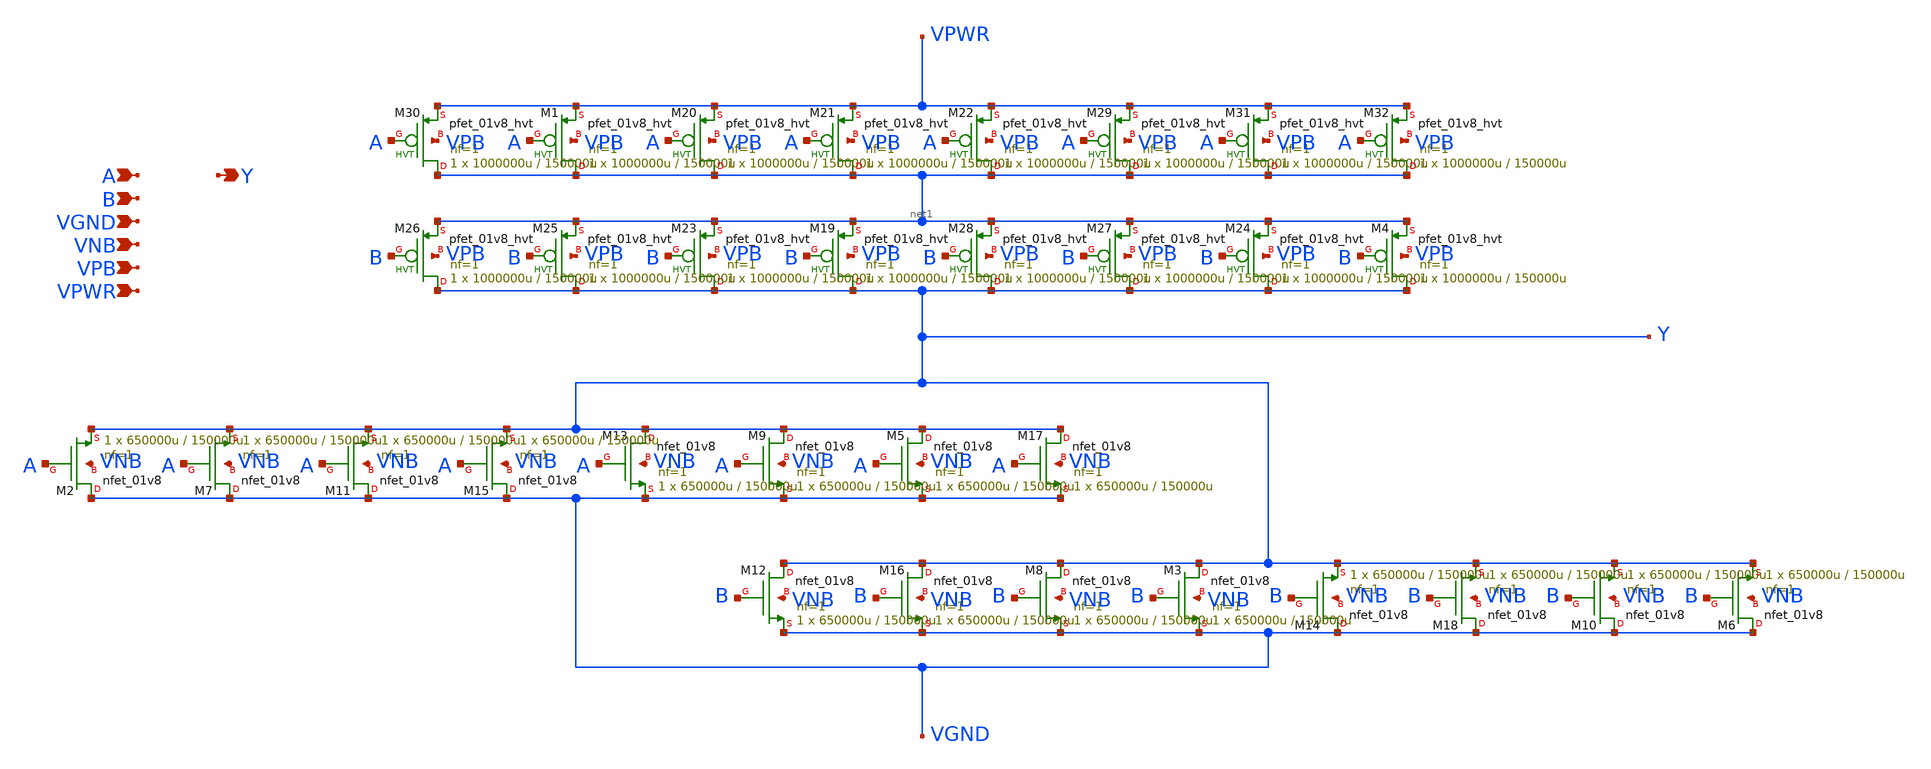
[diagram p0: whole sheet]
** sch_path: schematics/nor2/sky130_fd_sc_hd__nor2_8.sch
**.subckt sky130_fd_sc_hd__nor2_8 A B VGND VNB VPB VPWR Y
*.ipin A
*.ipin B
*.ipin VGND
*.ipin VNB
*.ipin VPB
*.ipin VPWR
*.opin Y
XM2 VGND A Y VNB sky130_fd_pr__nfet_01v8 L=150000u W=650000u nf=1 ad='int((1 + 1)/2) * 650000u / 1 * 0.29'
+ as='int((1 + 2)/2) * 650000u / 1 * 0.29' pd='2*int((1 + 1)/2) * (650000u / 1 + 0.29)' ps='2*int((1 + 2)/2) * (650000u / 1 + 0.29)'
+ nrd='0.29 / 650000u ' nrs='0.29 / 650000u ' sa=0 sb=0 sd=0 mult=1 m=1
XM3 Y B VGND VNB sky130_fd_pr__nfet_01v8 L=150000u W=650000u nf=1 ad='int((1 + 1)/2) * 650000u / 1 * 0.29'
+ as='int((1 + 2)/2) * 650000u / 1 * 0.29' pd='2*int((1 + 1)/2) * (650000u / 1 + 0.29)' ps='2*int((1 + 2)/2) * (650000u / 1 + 0.29)'
+ nrd='0.29 / 650000u ' nrs='0.29 / 650000u ' sa=0 sb=0 sd=0 mult=1 m=1
XM5 Y A VGND VNB sky130_fd_pr__nfet_01v8 L=150000u W=650000u nf=1 ad='int((1 + 1)/2) * 650000u / 1 * 0.29'
+ as='int((1 + 2)/2) * 650000u / 1 * 0.29' pd='2*int((1 + 1)/2) * (650000u / 1 + 0.29)' ps='2*int((1 + 2)/2) * (650000u / 1 + 0.29)'
+ nrd='0.29 / 650000u ' nrs='0.29 / 650000u ' sa=0 sb=0 sd=0 mult=1 m=1
XM6 VGND B Y VNB sky130_fd_pr__nfet_01v8 L=150000u W=650000u nf=1 ad='int((1 + 1)/2) * 650000u / 1 * 0.29'
+ as='int((1 + 2)/2) * 650000u / 1 * 0.29' pd='2*int((1 + 1)/2) * (650000u / 1 + 0.29)' ps='2*int((1 + 2)/2) * (650000u / 1 + 0.29)'
+ nrd='0.29 / 650000u ' nrs='0.29 / 650000u ' sa=0 sb=0 sd=0 mult=1 m=1
XM7 VGND A Y VNB sky130_fd_pr__nfet_01v8 L=150000u W=650000u nf=1 ad='int((1 + 1)/2) * 650000u / 1 * 0.29'
+ as='int((1 + 2)/2) * 650000u / 1 * 0.29' pd='2*int((1 + 1)/2) * (650000u / 1 + 0.29)' ps='2*int((1 + 2)/2) * (650000u / 1 + 0.29)'
+ nrd='0.29 / 650000u ' nrs='0.29 / 650000u ' sa=0 sb=0 sd=0 mult=1 m=1
XM8 Y B VGND VNB sky130_fd_pr__nfet_01v8 L=150000u W=650000u nf=1 ad='int((1 + 1)/2) * 650000u / 1 * 0.29'
+ as='int((1 + 2)/2) * 650000u / 1 * 0.29' pd='2*int((1 + 1)/2) * (650000u / 1 + 0.29)' ps='2*int((1 + 2)/2) * (650000u / 1 + 0.29)'
+ nrd='0.29 / 650000u ' nrs='0.29 / 650000u ' sa=0 sb=0 sd=0 mult=1 m=1
XM9 Y A VGND VNB sky130_fd_pr__nfet_01v8 L=150000u W=650000u nf=1 ad='int((1 + 1)/2) * 650000u / 1 * 0.29'
+ as='int((1 + 2)/2) * 650000u / 1 * 0.29' pd='2*int((1 + 1)/2) * (650000u / 1 + 0.29)' ps='2*int((1 + 2)/2) * (650000u / 1 + 0.29)'
+ nrd='0.29 / 650000u ' nrs='0.29 / 650000u ' sa=0 sb=0 sd=0 mult=1 m=1
XM10 VGND B Y VNB sky130_fd_pr__nfet_01v8 L=150000u W=650000u nf=1 ad='int((1 + 1)/2) * 650000u / 1 * 0.29'
+ as='int((1 + 2)/2) * 650000u / 1 * 0.29' pd='2*int((1 + 1)/2) * (650000u / 1 + 0.29)' ps='2*int((1 + 2)/2) * (650000u / 1 + 0.29)'
+ nrd='0.29 / 650000u ' nrs='0.29 / 650000u ' sa=0 sb=0 sd=0 mult=1 m=1
XM11 VGND A Y VNB sky130_fd_pr__nfet_01v8 L=150000u W=650000u nf=1 ad='int((1 + 1)/2) * 650000u / 1 * 0.29'
+ as='int((1 + 2)/2) * 650000u / 1 * 0.29' pd='2*int((1 + 1)/2) * (650000u / 1 + 0.29)' ps='2*int((1 + 2)/2) * (650000u / 1 + 0.29)'
+ nrd='0.29 / 650000u ' nrs='0.29 / 650000u ' sa=0 sb=0 sd=0 mult=1 m=1
XM12 Y B VGND VNB sky130_fd_pr__nfet_01v8 L=150000u W=650000u nf=1 ad='int((1 + 1)/2) * 650000u / 1 * 0.29'
+ as='int((1 + 2)/2) * 650000u / 1 * 0.29' pd='2*int((1 + 1)/2) * (650000u / 1 + 0.29)' ps='2*int((1 + 2)/2) * (650000u / 1 + 0.29)'
+ nrd='0.29 / 650000u ' nrs='0.29 / 650000u ' sa=0 sb=0 sd=0 mult=1 m=1
XM13 Y A VGND VNB sky130_fd_pr__nfet_01v8 L=150000u W=650000u nf=1 ad='int((1 + 1)/2) * 650000u / 1 * 0.29'
+ as='int((1 + 2)/2) * 650000u / 1 * 0.29' pd='2*int((1 + 1)/2) * (650000u / 1 + 0.29)' ps='2*int((1 + 2)/2) * (650000u / 1 + 0.29)'
+ nrd='0.29 / 650000u ' nrs='0.29 / 650000u ' sa=0 sb=0 sd=0 mult=1 m=1
XM14 VGND B Y VNB sky130_fd_pr__nfet_01v8 L=150000u W=650000u nf=1 ad='int((1 + 1)/2) * 650000u / 1 * 0.29'
+ as='int((1 + 2)/2) * 650000u / 1 * 0.29' pd='2*int((1 + 1)/2) * (650000u / 1 + 0.29)' ps='2*int((1 + 2)/2) * (650000u / 1 + 0.29)'
+ nrd='0.29 / 650000u ' nrs='0.29 / 650000u ' sa=0 sb=0 sd=0 mult=1 m=1
XM15 VGND A Y VNB sky130_fd_pr__nfet_01v8 L=150000u W=650000u nf=1 ad='int((1 + 1)/2) * 650000u / 1 * 0.29'
+ as='int((1 + 2)/2) * 650000u / 1 * 0.29' pd='2*int((1 + 1)/2) * (650000u / 1 + 0.29)' ps='2*int((1 + 2)/2) * (650000u / 1 + 0.29)'
+ nrd='0.29 / 650000u ' nrs='0.29 / 650000u ' sa=0 sb=0 sd=0 mult=1 m=1
XM16 Y B VGND VNB sky130_fd_pr__nfet_01v8 L=150000u W=650000u nf=1 ad='int((1 + 1)/2) * 650000u / 1 * 0.29'
+ as='int((1 + 2)/2) * 650000u / 1 * 0.29' pd='2*int((1 + 1)/2) * (650000u / 1 + 0.29)' ps='2*int((1 + 2)/2) * (650000u / 1 + 0.29)'
+ nrd='0.29 / 650000u ' nrs='0.29 / 650000u ' sa=0 sb=0 sd=0 mult=1 m=1
XM17 Y A VGND VNB sky130_fd_pr__nfet_01v8 L=150000u W=650000u nf=1 ad='int((1 + 1)/2) * 650000u / 1 * 0.29'
+ as='int((1 + 2)/2) * 650000u / 1 * 0.29' pd='2*int((1 + 1)/2) * (650000u / 1 + 0.29)' ps='2*int((1 + 2)/2) * (650000u / 1 + 0.29)'
+ nrd='0.29 / 650000u ' nrs='0.29 / 650000u ' sa=0 sb=0 sd=0 mult=1 m=1
XM18 VGND B Y VNB sky130_fd_pr__nfet_01v8 L=150000u W=650000u nf=1 ad='int((1 + 1)/2) * 650000u / 1 * 0.29'
+ as='int((1 + 2)/2) * 650000u / 1 * 0.29' pd='2*int((1 + 1)/2) * (650000u / 1 + 0.29)' ps='2*int((1 + 2)/2) * (650000u / 1 + 0.29)'
+ nrd='0.29 / 650000u ' nrs='0.29 / 650000u ' sa=0 sb=0 sd=0 mult=1 m=1
XM19 Y B net1 VPB sky130_fd_pr__pfet_01v8_hvt L=150000u W=1000000u nf=1 ad='int((1 + 1)/2) * 1000000u / 1 * 0.29'
+ as='int((1 + 2)/2) * 1000000u / 1 * 0.29' pd='2*int((1 + 1)/2) * (1000000u / 1 + 0.29)' ps='2*int((1 + 2)/2) * (1000000u / 1 + 0.29)'
+ nrd='0.29 / 1000000u ' nrs='0.29 / 1000000u ' sa=0 sb=0 sd=0 mult=1 m=1
XM23 Y B net1 VPB sky130_fd_pr__pfet_01v8_hvt L=150000u W=1000000u nf=1 ad='int((1 + 1)/2) * 1000000u / 1 * 0.29'
+ as='int((1 + 2)/2) * 1000000u / 1 * 0.29' pd='2*int((1 + 1)/2) * (1000000u / 1 + 0.29)' ps='2*int((1 + 2)/2) * (1000000u / 1 + 0.29)'
+ nrd='0.29 / 1000000u ' nrs='0.29 / 1000000u ' sa=0 sb=0 sd=0 mult=1 m=1
XM25 Y B net1 VPB sky130_fd_pr__pfet_01v8_hvt L=150000u W=1000000u nf=1 ad='int((1 + 1)/2) * 1000000u / 1 * 0.29'
+ as='int((1 + 2)/2) * 1000000u / 1 * 0.29' pd='2*int((1 + 1)/2) * (1000000u / 1 + 0.29)' ps='2*int((1 + 2)/2) * (1000000u / 1 + 0.29)'
+ nrd='0.29 / 1000000u ' nrs='0.29 / 1000000u ' sa=0 sb=0 sd=0 mult=1 m=1
XM26 Y B net1 VPB sky130_fd_pr__pfet_01v8_hvt L=150000u W=1000000u nf=1 ad='int((1 + 1)/2) * 1000000u / 1 * 0.29'
+ as='int((1 + 2)/2) * 1000000u / 1 * 0.29' pd='2*int((1 + 1)/2) * (1000000u / 1 + 0.29)' ps='2*int((1 + 2)/2) * (1000000u / 1 + 0.29)'
+ nrd='0.29 / 1000000u ' nrs='0.29 / 1000000u ' sa=0 sb=0 sd=0 mult=1 m=1
XM30 net1 A VPWR VPB sky130_fd_pr__pfet_01v8_hvt L=150000u W=1000000u nf=1 ad='int((1 + 1)/2) * 1000000u / 1 * 0.29'
+ as='int((1 + 2)/2) * 1000000u / 1 * 0.29' pd='2*int((1 + 1)/2) * (1000000u / 1 + 0.29)' ps='2*int((1 + 2)/2) * (1000000u / 1 + 0.29)'
+ nrd='0.29 / 1000000u ' nrs='0.29 / 1000000u ' sa=0 sb=0 sd=0 mult=1 m=1
XM4 Y B net1 VPB sky130_fd_pr__pfet_01v8_hvt L=150000u W=1000000u nf=1 ad='int((1 + 1)/2) * 1000000u / 1 * 0.29'
+ as='int((1 + 2)/2) * 1000000u / 1 * 0.29' pd='2*int((1 + 1)/2) * (1000000u / 1 + 0.29)' ps='2*int((1 + 2)/2) * (1000000u / 1 + 0.29)'
+ nrd='0.29 / 1000000u ' nrs='0.29 / 1000000u ' sa=0 sb=0 sd=0 mult=1 m=1
XM24 Y B net1 VPB sky130_fd_pr__pfet_01v8_hvt L=150000u W=1000000u nf=1 ad='int((1 + 1)/2) * 1000000u / 1 * 0.29'
+ as='int((1 + 2)/2) * 1000000u / 1 * 0.29' pd='2*int((1 + 1)/2) * (1000000u / 1 + 0.29)' ps='2*int((1 + 2)/2) * (1000000u / 1 + 0.29)'
+ nrd='0.29 / 1000000u ' nrs='0.29 / 1000000u ' sa=0 sb=0 sd=0 mult=1 m=1
XM27 Y B net1 VPB sky130_fd_pr__pfet_01v8_hvt L=150000u W=1000000u nf=1 ad='int((1 + 1)/2) * 1000000u / 1 * 0.29'
+ as='int((1 + 2)/2) * 1000000u / 1 * 0.29' pd='2*int((1 + 1)/2) * (1000000u / 1 + 0.29)' ps='2*int((1 + 2)/2) * (1000000u / 1 + 0.29)'
+ nrd='0.29 / 1000000u ' nrs='0.29 / 1000000u ' sa=0 sb=0 sd=0 mult=1 m=1
XM28 Y B net1 VPB sky130_fd_pr__pfet_01v8_hvt L=150000u W=1000000u nf=1 ad='int((1 + 1)/2) * 1000000u / 1 * 0.29'
+ as='int((1 + 2)/2) * 1000000u / 1 * 0.29' pd='2*int((1 + 1)/2) * (1000000u / 1 + 0.29)' ps='2*int((1 + 2)/2) * (1000000u / 1 + 0.29)'
+ nrd='0.29 / 1000000u ' nrs='0.29 / 1000000u ' sa=0 sb=0 sd=0 mult=1 m=1
XM1 net1 A VPWR VPB sky130_fd_pr__pfet_01v8_hvt L=150000u W=1000000u nf=1 ad='int((1 + 1)/2) * 1000000u / 1 * 0.29'
+ as='int((1 + 2)/2) * 1000000u / 1 * 0.29' pd='2*int((1 + 1)/2) * (1000000u / 1 + 0.29)' ps='2*int((1 + 2)/2) * (1000000u / 1 + 0.29)'
+ nrd='0.29 / 1000000u ' nrs='0.29 / 1000000u ' sa=0 sb=0 sd=0 mult=1 m=1
XM20 net1 A VPWR VPB sky130_fd_pr__pfet_01v8_hvt L=150000u W=1000000u nf=1 ad='int((1 + 1)/2) * 1000000u / 1 * 0.29'
+ as='int((1 + 2)/2) * 1000000u / 1 * 0.29' pd='2*int((1 + 1)/2) * (1000000u / 1 + 0.29)' ps='2*int((1 + 2)/2) * (1000000u / 1 + 0.29)'
+ nrd='0.29 / 1000000u ' nrs='0.29 / 1000000u ' sa=0 sb=0 sd=0 mult=1 m=1
XM21 net1 A VPWR VPB sky130_fd_pr__pfet_01v8_hvt L=150000u W=1000000u nf=1 ad='int((1 + 1)/2) * 1000000u / 1 * 0.29'
+ as='int((1 + 2)/2) * 1000000u / 1 * 0.29' pd='2*int((1 + 1)/2) * (1000000u / 1 + 0.29)' ps='2*int((1 + 2)/2) * (1000000u / 1 + 0.29)'
+ nrd='0.29 / 1000000u ' nrs='0.29 / 1000000u ' sa=0 sb=0 sd=0 mult=1 m=1
XM22 net1 A VPWR VPB sky130_fd_pr__pfet_01v8_hvt L=150000u W=1000000u nf=1 ad='int((1 + 1)/2) * 1000000u / 1 * 0.29'
+ as='int((1 + 2)/2) * 1000000u / 1 * 0.29' pd='2*int((1 + 1)/2) * (1000000u / 1 + 0.29)' ps='2*int((1 + 2)/2) * (1000000u / 1 + 0.29)'
+ nrd='0.29 / 1000000u ' nrs='0.29 / 1000000u ' sa=0 sb=0 sd=0 mult=1 m=1
XM29 net1 A VPWR VPB sky130_fd_pr__pfet_01v8_hvt L=150000u W=1000000u nf=1 ad='int((1 + 1)/2) * 1000000u / 1 * 0.29'
+ as='int((1 + 2)/2) * 1000000u / 1 * 0.29' pd='2*int((1 + 1)/2) * (1000000u / 1 + 0.29)' ps='2*int((1 + 2)/2) * (1000000u / 1 + 0.29)'
+ nrd='0.29 / 1000000u ' nrs='0.29 / 1000000u ' sa=0 sb=0 sd=0 mult=1 m=1
XM31 net1 A VPWR VPB sky130_fd_pr__pfet_01v8_hvt L=150000u W=1000000u nf=1 ad='int((1 + 1)/2) * 1000000u / 1 * 0.29'
+ as='int((1 + 2)/2) * 1000000u / 1 * 0.29' pd='2*int((1 + 1)/2) * (1000000u / 1 + 0.29)' ps='2*int((1 + 2)/2) * (1000000u / 1 + 0.29)'
+ nrd='0.29 / 1000000u ' nrs='0.29 / 1000000u ' sa=0 sb=0 sd=0 mult=1 m=1
XM32 net1 A VPWR VPB sky130_fd_pr__pfet_01v8_hvt L=150000u W=1000000u nf=1 ad='int((1 + 1)/2) * 1000000u / 1 * 0.29'
+ as='int((1 + 2)/2) * 1000000u / 1 * 0.29' pd='2*int((1 + 1)/2) * (1000000u / 1 + 0.29)' ps='2*int((1 + 2)/2) * (1000000u / 1 + 0.29)'
+ nrd='0.29 / 1000000u ' nrs='0.29 / 1000000u ' sa=0 sb=0 sd=0 mult=1 m=1
**.ends
.end
